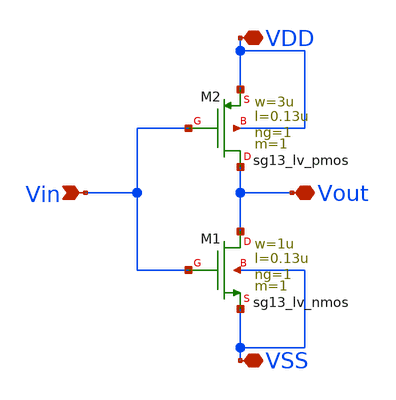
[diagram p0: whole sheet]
** sch_path: inverter_tutorial/xschem/inverter.sch
**.subckt inverter Vin VDD Vout VSS
*.ipin Vin
*.iopin VDD
*.iopin Vout
*.iopin VSS
XM1 Vout Vin VSS VSS sg13_lv_nmos w=1u l=0.13u ng=1 m=1 mm_ok=1
XM2 Vout Vin VDD VDD sg13_lv_pmos w=3u l=0.13u ng=1 m=1 mm_ok=1
**.ends
.end
